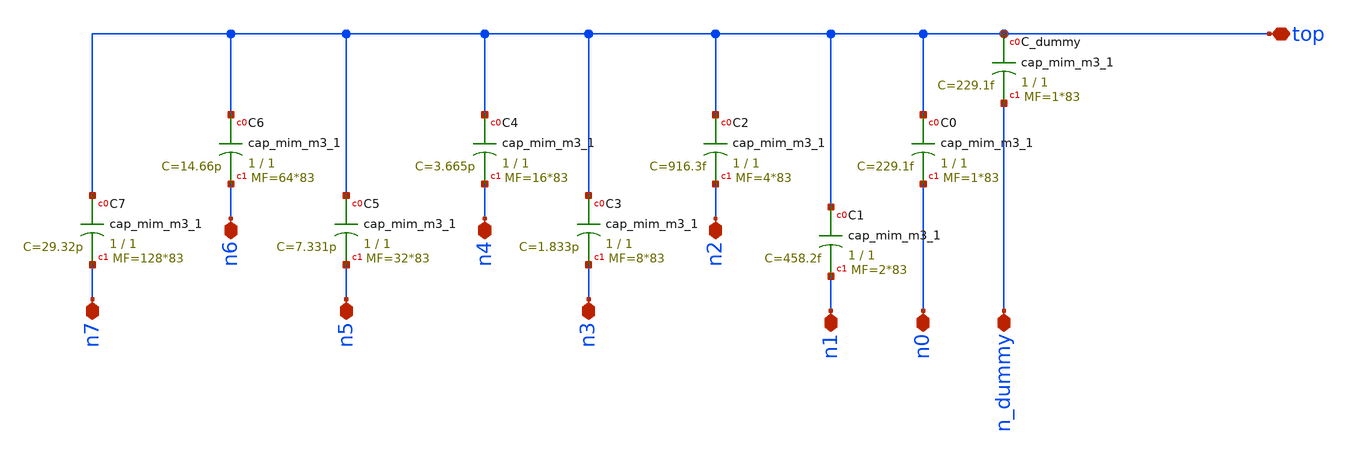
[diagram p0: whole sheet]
** sch_path: Schematics/ADC/c_array/c_array.sch
**.subckt c_array n1 n0 n_dummy top n2 n3 n4 n5 n6 n7
*.iopin n1
*.iopin n0
*.iopin n_dummy
*.iopin top
*.iopin n2
*.iopin n3
*.iopin n4
*.iopin n5
*.iopin n6
*.iopin n7
XC0 top n0 sky130_fd_pr__cap_mim_m3_1 W=1 L=1 MF=1*83 m=1*83
XC_dummy top n_dummy sky130_fd_pr__cap_mim_m3_1 W=1 L=1 MF=1*83 m=1*83
XC1 top n1 sky130_fd_pr__cap_mim_m3_1 W=1 L=1 MF=2*83 m=2*83
XC2 top n2 sky130_fd_pr__cap_mim_m3_1 W=1 L=1 MF=4*83 m=4*83
XC3 top n3 sky130_fd_pr__cap_mim_m3_1 W=1 L=1 MF=8*83 m=8*83
XC4 top n4 sky130_fd_pr__cap_mim_m3_1 W=1 L=1 MF=16*83 m=16*83
XC5 top n5 sky130_fd_pr__cap_mim_m3_1 W=1 L=1 MF=32*83 m=32*83
XC6 top n6 sky130_fd_pr__cap_mim_m3_1 W=1 L=1 MF=64*83 m=64*83
XC7 top n7 sky130_fd_pr__cap_mim_m3_1 W=1 L=1 MF=128*83 m=128*83
**.ends
.end
